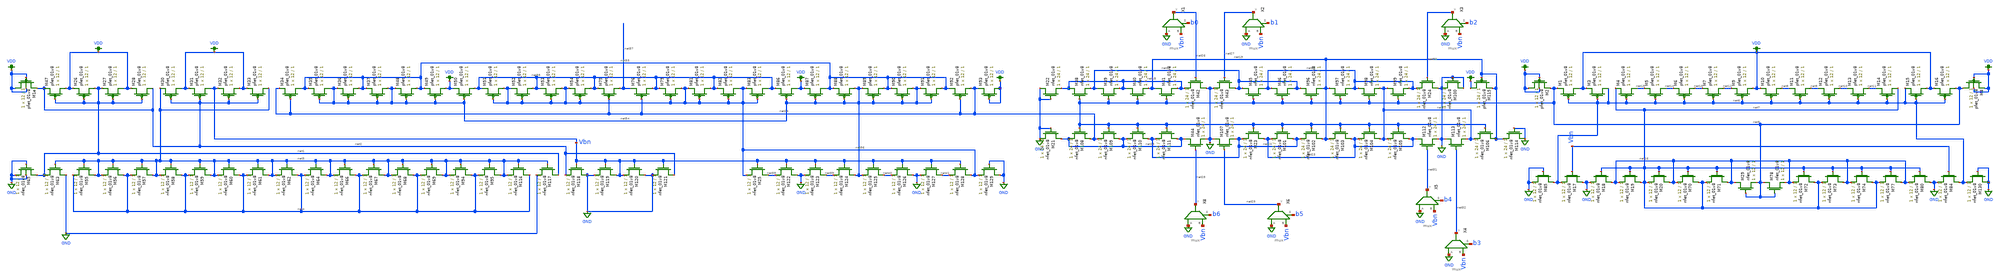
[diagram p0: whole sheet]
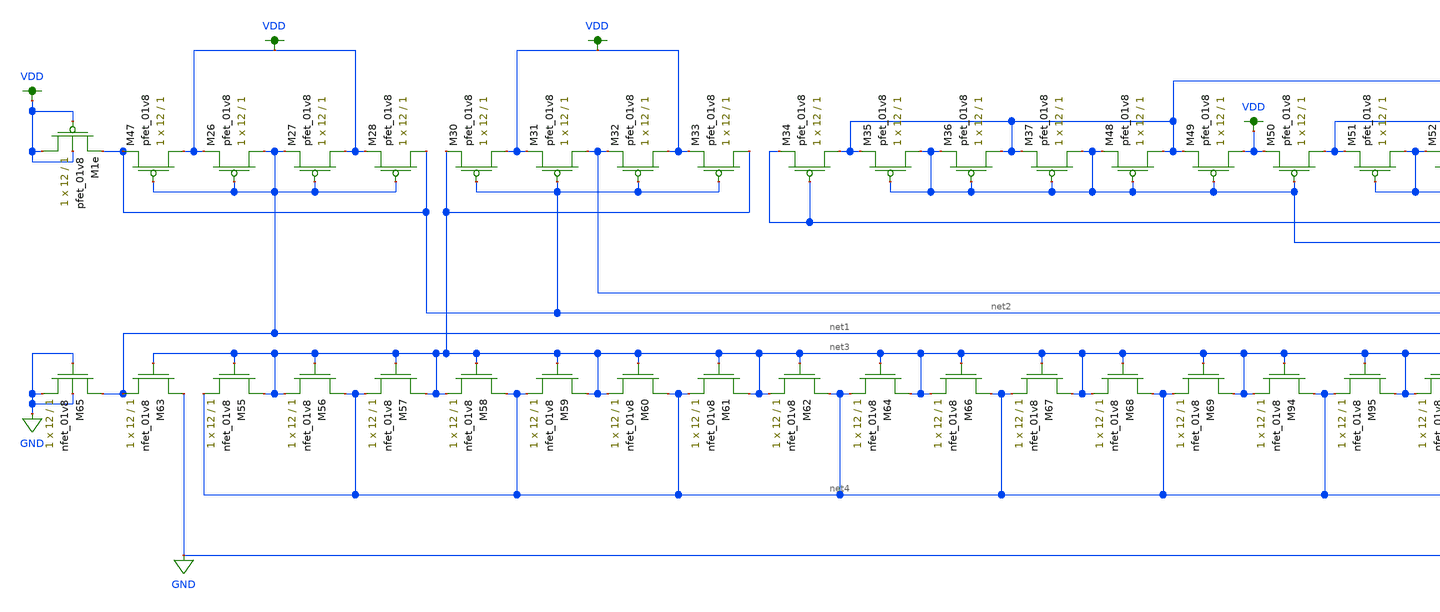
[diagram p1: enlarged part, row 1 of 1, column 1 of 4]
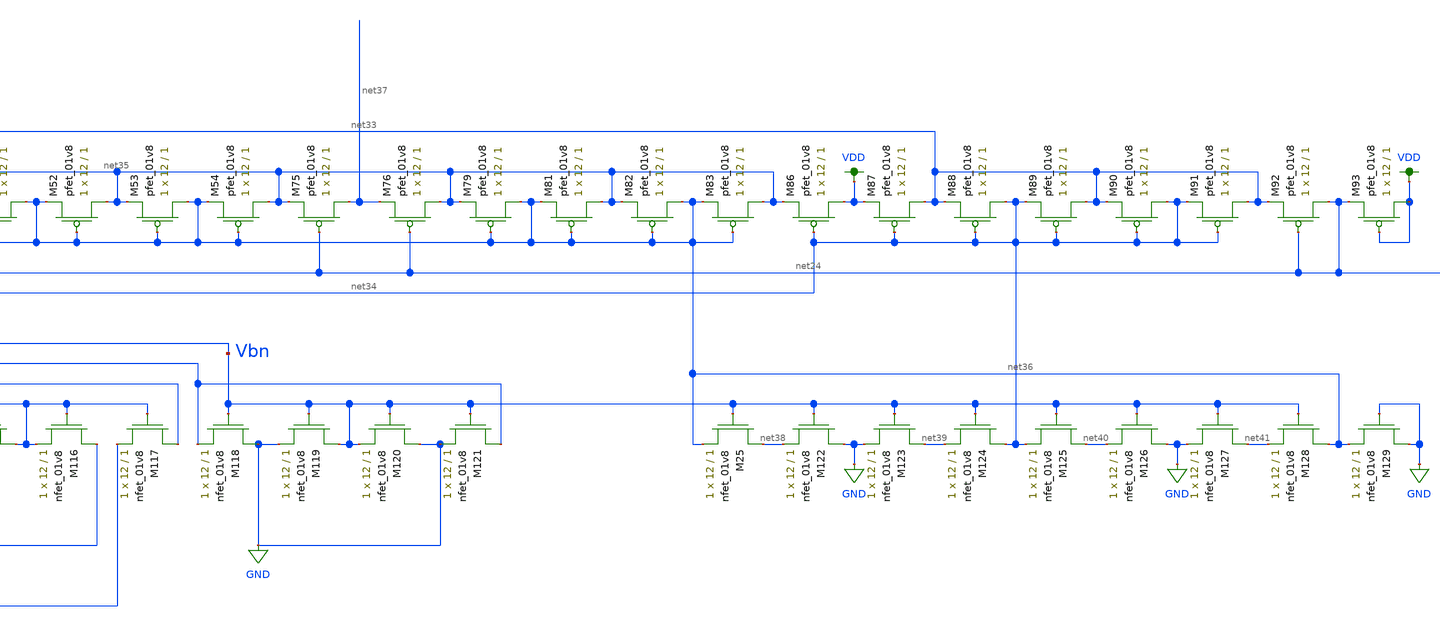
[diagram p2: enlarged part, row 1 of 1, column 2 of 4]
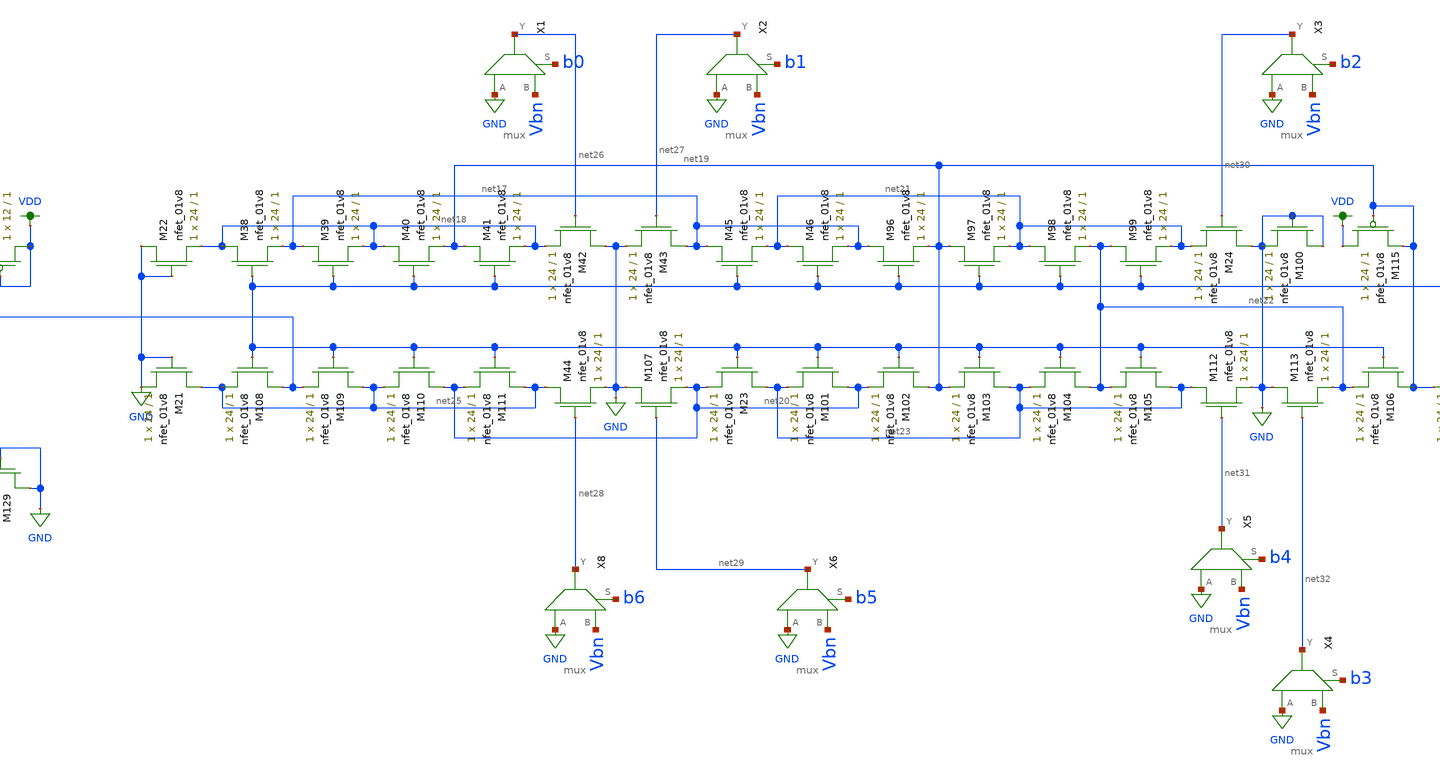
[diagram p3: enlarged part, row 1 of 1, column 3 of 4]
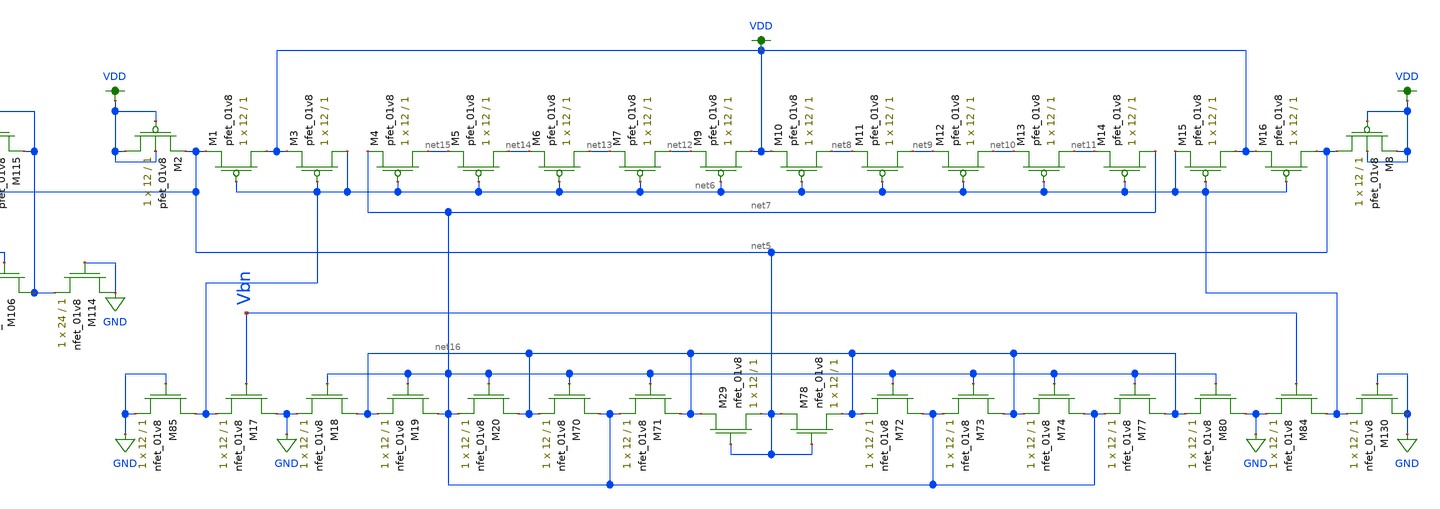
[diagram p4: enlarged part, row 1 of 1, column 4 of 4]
** sch_path: dac/schematics/lds_for_lvs.sch
**.subckt lds_for_lvs
XM47 VDD net1 net2 VDD sky130_fd_pr__pfet_01v8 L=1 W=12 nf=1 ad='int((nf+1)/2) * W/nf * 0.29' as='int((nf+2)/2) * W/nf * 0.29'
+ pd='2*int((nf+1)/2) * (W/nf + 0.29)' ps='2*int((nf+2)/2) * (W/nf + 0.29)' nrd='0.29 / W' nrs='0.29 / W'
+ sa=0 sb=0 sd=0 mult=1 m=1
XM63 GND net3 net1 GND sky130_fd_pr__nfet_01v8 L=1 W=12 nf=1 ad='int((nf+1)/2) * W/nf * 0.29' as='int((nf+2)/2) * W/nf * 0.29'
+ pd='2*int((nf+1)/2) * (W/nf + 0.29)' ps='2*int((nf+2)/2) * (W/nf + 0.29)' nrd='0.29 / W' nrs='0.29 / W'
+ sa=0 sb=0 sd=0 mult=1 m=1
XM1e VDD VDD net2 VDD sky130_fd_pr__pfet_01v8 L=1 W=12 nf=1 ad='int((nf+1)/2) * W/nf * 0.29' as='int((nf+2)/2) * W/nf * 0.29'
+ pd='2*int((nf+1)/2) * (W/nf + 0.29)' ps='2*int((nf+2)/2) * (W/nf + 0.29)' nrd='0.29 / W' nrs='0.29 / W'
+ sa=0 sb=0 sd=0 mult=1 m=1
XM65 net1 GND GND GND sky130_fd_pr__nfet_01v8 L=1 W=12 nf=1 ad='int((nf+1)/2) * W/nf * 0.29' as='int((nf+2)/2) * W/nf * 0.29'
+ pd='2*int((nf+1)/2) * (W/nf + 0.29)' ps='2*int((nf+2)/2) * (W/nf + 0.29)' nrd='0.29 / W' nrs='0.29 / W'
+ sa=0 sb=0 sd=0 mult=1 m=1
XM1 VDD net6 net5 VDD sky130_fd_pr__pfet_01v8 L=1 W=12 nf=1 ad='int((nf+1)/2) * W/nf * 0.29' as='int((nf+2)/2) * W/nf * 0.29'
+ pd='2*int((nf+1)/2) * (W/nf + 0.29)' ps='2*int((nf+2)/2) * (W/nf + 0.29)' nrd='0.29 / W' nrs='0.29 / W'
+ sa=0 sb=0 sd=0 mult=1 m=1
XM2 VDD VDD net5 VDD sky130_fd_pr__pfet_01v8 L=1 W=12 nf=1 ad='int((nf+1)/2) * W/nf * 0.29' as='int((nf+2)/2) * W/nf * 0.29'
+ pd='2*int((nf+1)/2) * (W/nf + 0.29)' ps='2*int((nf+2)/2) * (W/nf + 0.29)' nrd='0.29 / W' nrs='0.29 / W'
+ sa=0 sb=0 sd=0 mult=1 m=1
XM85 net6 GND GND GND sky130_fd_pr__nfet_01v8 L=1 W=12 nf=1 ad='int((nf+1)/2) * W/nf * 0.29' as='int((nf+2)/2) * W/nf * 0.29'
+ pd='2*int((nf+1)/2) * (W/nf + 0.29)' ps='2*int((nf+2)/2) * (W/nf + 0.29)' nrd='0.29 / W' nrs='0.29 / W'
+ sa=0 sb=0 sd=0 mult=1 m=1
X1 GND Vbn net26 b0 mux
X2 GND Vbn net27 b1 mux
X3 GND Vbn net30 b2 mux
X4 GND Vbn net32 b3 mux
X5 GND Vbn net31 b4 mux
X6 GND Vbn net29 b5 mux
X8 GND Vbn net28 b6 mux
XM115 VDD net19 net19 VDD sky130_fd_pr__pfet_01v8 L=1 W=24 nf=1 ad='int((nf+1)/2) * W/nf * 0.29' as='int((nf+2)/2) * W/nf * 0.29'
+ pd='2*int((nf+1)/2) * (W/nf + 0.29)' ps='2*int((nf+2)/2) * (W/nf + 0.29)' nrd='0.29 / W' nrs='0.29 / W'
+ sa=0 sb=0 sd=0 mult=1 m=1
XM22 GND GND net18 GND sky130_fd_pr__nfet_01v8 L=1 W=24 nf=1 ad='int((nf+1)/2) * W/nf * 0.29' as='int((nf+2)/2) * W/nf * 0.29'
+ pd='2*int((nf+1)/2) * (W/nf + 0.29)' ps='2*int((nf+2)/2) * (W/nf + 0.29)' nrd='0.29 / W' nrs='0.29 / W'
+ sa=0 sb=0 sd=0 mult=1 m=1
XM26 net1 net1 VDD VDD sky130_fd_pr__pfet_01v8 L=1 W=12 nf=1 ad='int((nf+1)/2) * W/nf * 0.29' as='int((nf+2)/2) * W/nf * 0.29'
+ pd='2*int((nf+1)/2) * (W/nf + 0.29)' ps='2*int((nf+2)/2) * (W/nf + 0.29)' nrd='0.29 / W' nrs='0.29 / W'
+ sa=0 sb=0 sd=0 mult=1 m=1
XM27 VDD net1 net1 VDD sky130_fd_pr__pfet_01v8 L=1 W=12 nf=1 ad='int((nf+1)/2) * W/nf * 0.29' as='int((nf+2)/2) * W/nf * 0.29'
+ pd='2*int((nf+1)/2) * (W/nf + 0.29)' ps='2*int((nf+2)/2) * (W/nf + 0.29)' nrd='0.29 / W' nrs='0.29 / W'
+ sa=0 sb=0 sd=0 mult=1 m=1
XM28 net2 net1 VDD VDD sky130_fd_pr__pfet_01v8 L=1 W=12 nf=1 ad='int((nf+1)/2) * W/nf * 0.29' as='int((nf+2)/2) * W/nf * 0.29'
+ pd='2*int((nf+1)/2) * (W/nf + 0.29)' ps='2*int((nf+2)/2) * (W/nf + 0.29)' nrd='0.29 / W' nrs='0.29 / W'
+ sa=0 sb=0 sd=0 mult=1 m=1
XM30 VDD net2 net3 VDD sky130_fd_pr__pfet_01v8 L=1 W=12 nf=1 ad='int((nf+1)/2) * W/nf * 0.29' as='int((nf+2)/2) * W/nf * 0.29'
+ pd='2*int((nf+1)/2) * (W/nf + 0.29)' ps='2*int((nf+2)/2) * (W/nf + 0.29)' nrd='0.29 / W' nrs='0.29 / W'
+ sa=0 sb=0 sd=0 mult=1 m=1
XM31 Vbn net2 VDD VDD sky130_fd_pr__pfet_01v8 L=1 W=12 nf=1 ad='int((nf+1)/2) * W/nf * 0.29' as='int((nf+2)/2) * W/nf * 0.29'
+ pd='2*int((nf+1)/2) * (W/nf + 0.29)' ps='2*int((nf+2)/2) * (W/nf + 0.29)' nrd='0.29 / W' nrs='0.29 / W'
+ sa=0 sb=0 sd=0 mult=1 m=1
XM32 VDD net2 Vbn VDD sky130_fd_pr__pfet_01v8 L=1 W=12 nf=1 ad='int((nf+1)/2) * W/nf * 0.29' as='int((nf+2)/2) * W/nf * 0.29'
+ pd='2*int((nf+1)/2) * (W/nf + 0.29)' ps='2*int((nf+2)/2) * (W/nf + 0.29)' nrd='0.29 / W' nrs='0.29 / W'
+ sa=0 sb=0 sd=0 mult=1 m=1
XM33 net3 net2 VDD VDD sky130_fd_pr__pfet_01v8 L=1 W=12 nf=1 ad='int((nf+1)/2) * W/nf * 0.29' as='int((nf+2)/2) * W/nf * 0.29'
+ pd='2*int((nf+1)/2) * (W/nf + 0.29)' ps='2*int((nf+2)/2) * (W/nf + 0.29)' nrd='0.29 / W' nrs='0.29 / W'
+ sa=0 sb=0 sd=0 mult=1 m=1
XM34 net33 net24 net24 VDD sky130_fd_pr__pfet_01v8 L=1 W=12 nf=1 ad='int((nf+1)/2) * W/nf * 0.29' as='int((nf+2)/2) * W/nf * 0.29'
+ pd='2*int((nf+1)/2) * (W/nf + 0.29)' ps='2*int((nf+2)/2) * (W/nf + 0.29)' nrd='0.29 / W' nrs='0.29 / W'
+ sa=0 sb=0 sd=0 mult=1 m=1
XM35 net34 net34 net33 VDD sky130_fd_pr__pfet_01v8 L=1 W=12 nf=1 ad='int((nf+1)/2) * W/nf * 0.29' as='int((nf+2)/2) * W/nf * 0.29'
+ pd='2*int((nf+1)/2) * (W/nf + 0.29)' ps='2*int((nf+2)/2) * (W/nf + 0.29)' nrd='0.29 / W' nrs='0.29 / W'
+ sa=0 sb=0 sd=0 mult=1 m=1
XM36 net33 net34 net34 VDD sky130_fd_pr__pfet_01v8 L=1 W=12 nf=1 ad='int((nf+1)/2) * W/nf * 0.29' as='int((nf+2)/2) * W/nf * 0.29'
+ pd='2*int((nf+1)/2) * (W/nf + 0.29)' ps='2*int((nf+2)/2) * (W/nf + 0.29)' nrd='0.29 / W' nrs='0.29 / W'
+ sa=0 sb=0 sd=0 mult=1 m=1
XM37 net34 net34 net33 VDD sky130_fd_pr__pfet_01v8 L=1 W=12 nf=1 ad='int((nf+1)/2) * W/nf * 0.29' as='int((nf+2)/2) * W/nf * 0.29'
+ pd='2*int((nf+1)/2) * (W/nf + 0.29)' ps='2*int((nf+2)/2) * (W/nf + 0.29)' nrd='0.29 / W' nrs='0.29 / W'
+ sa=0 sb=0 sd=0 mult=1 m=1
XM48 net33 net34 net34 VDD sky130_fd_pr__pfet_01v8 L=1 W=12 nf=1 ad='int((nf+1)/2) * W/nf * 0.29' as='int((nf+2)/2) * W/nf * 0.29'
+ pd='2*int((nf+1)/2) * (W/nf + 0.29)' ps='2*int((nf+2)/2) * (W/nf + 0.29)' nrd='0.29 / W' nrs='0.29 / W'
+ sa=0 sb=0 sd=0 mult=1 m=1
XM49 VDD net34 net33 VDD sky130_fd_pr__pfet_01v8 L=1 W=12 nf=1 ad='int((nf+1)/2) * W/nf * 0.29' as='int((nf+2)/2) * W/nf * 0.29'
+ pd='2*int((nf+1)/2) * (W/nf + 0.29)' ps='2*int((nf+2)/2) * (W/nf + 0.29)' nrd='0.29 / W' nrs='0.29 / W'
+ sa=0 sb=0 sd=0 mult=1 m=1
XM50 net35 net34 VDD VDD sky130_fd_pr__pfet_01v8 L=1 W=12 nf=1 ad='int((nf+1)/2) * W/nf * 0.29' as='int((nf+2)/2) * W/nf * 0.29'
+ pd='2*int((nf+1)/2) * (W/nf + 0.29)' ps='2*int((nf+2)/2) * (W/nf + 0.29)' nrd='0.29 / W' nrs='0.29 / W'
+ sa=0 sb=0 sd=0 mult=1 m=1
XM51 net36 net36 net35 VDD sky130_fd_pr__pfet_01v8 L=1 W=12 nf=1 ad='int((nf+1)/2) * W/nf * 0.29' as='int((nf+2)/2) * W/nf * 0.29'
+ pd='2*int((nf+1)/2) * (W/nf + 0.29)' ps='2*int((nf+2)/2) * (W/nf + 0.29)' nrd='0.29 / W' nrs='0.29 / W'
+ sa=0 sb=0 sd=0 mult=1 m=1
XM52 net35 net36 net36 VDD sky130_fd_pr__pfet_01v8 L=1 W=12 nf=1 ad='int((nf+1)/2) * W/nf * 0.29' as='int((nf+2)/2) * W/nf * 0.29'
+ pd='2*int((nf+1)/2) * (W/nf + 0.29)' ps='2*int((nf+2)/2) * (W/nf + 0.29)' nrd='0.29 / W' nrs='0.29 / W'
+ sa=0 sb=0 sd=0 mult=1 m=1
XM53 net36 net36 net35 VDD sky130_fd_pr__pfet_01v8 L=1 W=12 nf=1 ad='int((nf+1)/2) * W/nf * 0.29' as='int((nf+2)/2) * W/nf * 0.29'
+ pd='2*int((nf+1)/2) * (W/nf + 0.29)' ps='2*int((nf+2)/2) * (W/nf + 0.29)' nrd='0.29 / W' nrs='0.29 / W'
+ sa=0 sb=0 sd=0 mult=1 m=1
XM54 net35 net36 net36 VDD sky130_fd_pr__pfet_01v8 L=1 W=12 nf=1 ad='int((nf+1)/2) * W/nf * 0.29' as='int((nf+2)/2) * W/nf * 0.29'
+ pd='2*int((nf+1)/2) * (W/nf + 0.29)' ps='2*int((nf+2)/2) * (W/nf + 0.29)' nrd='0.29 / W' nrs='0.29 / W'
+ sa=0 sb=0 sd=0 mult=1 m=1
XM75 net37 net24 net35 VDD sky130_fd_pr__pfet_01v8 L=1 W=12 nf=1 ad='int((nf+1)/2) * W/nf * 0.29' as='int((nf+2)/2) * W/nf * 0.29'
+ pd='2*int((nf+1)/2) * (W/nf + 0.29)' ps='2*int((nf+2)/2) * (W/nf + 0.29)' nrd='0.29 / W' nrs='0.29 / W'
+ sa=0 sb=0 sd=0 mult=1 m=1
XM76 net35 net24 net37 VDD sky130_fd_pr__pfet_01v8 L=1 W=12 nf=1 ad='int((nf+1)/2) * W/nf * 0.29' as='int((nf+2)/2) * W/nf * 0.29'
+ pd='2*int((nf+1)/2) * (W/nf + 0.29)' ps='2*int((nf+2)/2) * (W/nf + 0.29)' nrd='0.29 / W' nrs='0.29 / W'
+ sa=0 sb=0 sd=0 mult=1 m=1
XM79 net36 net36 net35 VDD sky130_fd_pr__pfet_01v8 L=1 W=12 nf=1 ad='int((nf+1)/2) * W/nf * 0.29' as='int((nf+2)/2) * W/nf * 0.29'
+ pd='2*int((nf+1)/2) * (W/nf + 0.29)' ps='2*int((nf+2)/2) * (W/nf + 0.29)' nrd='0.29 / W' nrs='0.29 / W'
+ sa=0 sb=0 sd=0 mult=1 m=1
XM81 net35 net36 net36 VDD sky130_fd_pr__pfet_01v8 L=1 W=12 nf=1 ad='int((nf+1)/2) * W/nf * 0.29' as='int((nf+2)/2) * W/nf * 0.29'
+ pd='2*int((nf+1)/2) * (W/nf + 0.29)' ps='2*int((nf+2)/2) * (W/nf + 0.29)' nrd='0.29 / W' nrs='0.29 / W'
+ sa=0 sb=0 sd=0 mult=1 m=1
XM82 net36 net36 net35 VDD sky130_fd_pr__pfet_01v8 L=1 W=12 nf=1 ad='int((nf+1)/2) * W/nf * 0.29' as='int((nf+2)/2) * W/nf * 0.29'
+ pd='2*int((nf+1)/2) * (W/nf + 0.29)' ps='2*int((nf+2)/2) * (W/nf + 0.29)' nrd='0.29 / W' nrs='0.29 / W'
+ sa=0 sb=0 sd=0 mult=1 m=1
XM83 net35 net36 net36 VDD sky130_fd_pr__pfet_01v8 L=1 W=12 nf=1 ad='int((nf+1)/2) * W/nf * 0.29' as='int((nf+2)/2) * W/nf * 0.29'
+ pd='2*int((nf+1)/2) * (W/nf + 0.29)' ps='2*int((nf+2)/2) * (W/nf + 0.29)' nrd='0.29 / W' nrs='0.29 / W'
+ sa=0 sb=0 sd=0 mult=1 m=1
XM86 VDD net34 net35 VDD sky130_fd_pr__pfet_01v8 L=1 W=12 nf=1 ad='int((nf+1)/2) * W/nf * 0.29' as='int((nf+2)/2) * W/nf * 0.29'
+ pd='2*int((nf+1)/2) * (W/nf + 0.29)' ps='2*int((nf+2)/2) * (W/nf + 0.29)' nrd='0.29 / W' nrs='0.29 / W'
+ sa=0 sb=0 sd=0 mult=1 m=1
XM87 net33 net34 VDD VDD sky130_fd_pr__pfet_01v8 L=1 W=12 nf=1 ad='int((nf+1)/2) * W/nf * 0.29' as='int((nf+2)/2) * W/nf * 0.29'
+ pd='2*int((nf+1)/2) * (W/nf + 0.29)' ps='2*int((nf+2)/2) * (W/nf + 0.29)' nrd='0.29 / W' nrs='0.29 / W'
+ sa=0 sb=0 sd=0 mult=1 m=1
XM88 net34 net34 net33 VDD sky130_fd_pr__pfet_01v8 L=1 W=12 nf=1 ad='int((nf+1)/2) * W/nf * 0.29' as='int((nf+2)/2) * W/nf * 0.29'
+ pd='2*int((nf+1)/2) * (W/nf + 0.29)' ps='2*int((nf+2)/2) * (W/nf + 0.29)' nrd='0.29 / W' nrs='0.29 / W'
+ sa=0 sb=0 sd=0 mult=1 m=1
XM89 net33 net34 net34 VDD sky130_fd_pr__pfet_01v8 L=1 W=12 nf=1 ad='int((nf+1)/2) * W/nf * 0.29' as='int((nf+2)/2) * W/nf * 0.29'
+ pd='2*int((nf+1)/2) * (W/nf + 0.29)' ps='2*int((nf+2)/2) * (W/nf + 0.29)' nrd='0.29 / W' nrs='0.29 / W'
+ sa=0 sb=0 sd=0 mult=1 m=1
XM90 net34 net34 net33 VDD sky130_fd_pr__pfet_01v8 L=1 W=12 nf=1 ad='int((nf+1)/2) * W/nf * 0.29' as='int((nf+2)/2) * W/nf * 0.29'
+ pd='2*int((nf+1)/2) * (W/nf + 0.29)' ps='2*int((nf+2)/2) * (W/nf + 0.29)' nrd='0.29 / W' nrs='0.29 / W'
+ sa=0 sb=0 sd=0 mult=1 m=1
XM91 net33 net34 net34 VDD sky130_fd_pr__pfet_01v8 L=1 W=12 nf=1 ad='int((nf+1)/2) * W/nf * 0.29' as='int((nf+2)/2) * W/nf * 0.29'
+ pd='2*int((nf+1)/2) * (W/nf + 0.29)' ps='2*int((nf+2)/2) * (W/nf + 0.29)' nrd='0.29 / W' nrs='0.29 / W'
+ sa=0 sb=0 sd=0 mult=1 m=1
XM92 net24 net24 net33 VDD sky130_fd_pr__pfet_01v8 L=1 W=12 nf=1 ad='int((nf+1)/2) * W/nf * 0.29' as='int((nf+2)/2) * W/nf * 0.29'
+ pd='2*int((nf+1)/2) * (W/nf + 0.29)' ps='2*int((nf+2)/2) * (W/nf + 0.29)' nrd='0.29 / W' nrs='0.29 / W'
+ sa=0 sb=0 sd=0 mult=1 m=1
XM93 VDD VDD net24 VDD sky130_fd_pr__pfet_01v8 L=1 W=12 nf=1 ad='int((nf+1)/2) * W/nf * 0.29' as='int((nf+2)/2) * W/nf * 0.29'
+ pd='2*int((nf+1)/2) * (W/nf + 0.29)' ps='2*int((nf+2)/2) * (W/nf + 0.29)' nrd='0.29 / W' nrs='0.29 / W'
+ sa=0 sb=0 sd=0 mult=1 m=1
XM8 net5 VDD VDD VDD sky130_fd_pr__pfet_01v8 L=1 W=12 nf=1 ad='int((nf+1)/2) * W/nf * 0.29' as='int((nf+2)/2) * W/nf * 0.29'
+ pd='2*int((nf+1)/2) * (W/nf + 0.29)' ps='2*int((nf+2)/2) * (W/nf + 0.29)' nrd='0.29 / W' nrs='0.29 / W'
+ sa=0 sb=0 sd=0 mult=1 m=1
XM3 net6 net6 VDD VDD sky130_fd_pr__pfet_01v8 L=1 W=12 nf=1 ad='int((nf+1)/2) * W/nf * 0.29' as='int((nf+2)/2) * W/nf * 0.29'
+ pd='2*int((nf+1)/2) * (W/nf + 0.29)' ps='2*int((nf+2)/2) * (W/nf + 0.29)' nrd='0.29 / W' nrs='0.29 / W'
+ sa=0 sb=0 sd=0 mult=1 m=1
XM4 net15 net6 net7 VDD sky130_fd_pr__pfet_01v8 L=1 W=12 nf=1 ad='int((nf+1)/2) * W/nf * 0.29' as='int((nf+2)/2) * W/nf * 0.29'
+ pd='2*int((nf+1)/2) * (W/nf + 0.29)' ps='2*int((nf+2)/2) * (W/nf + 0.29)' nrd='0.29 / W' nrs='0.29 / W'
+ sa=0 sb=0 sd=0 mult=1 m=1
XM5 net14 net6 net15 VDD sky130_fd_pr__pfet_01v8 L=1 W=12 nf=1 ad='int((nf+1)/2) * W/nf * 0.29' as='int((nf+2)/2) * W/nf * 0.29'
+ pd='2*int((nf+1)/2) * (W/nf + 0.29)' ps='2*int((nf+2)/2) * (W/nf + 0.29)' nrd='0.29 / W' nrs='0.29 / W'
+ sa=0 sb=0 sd=0 mult=1 m=1
XM6 net13 net6 net14 VDD sky130_fd_pr__pfet_01v8 L=1 W=12 nf=1 ad='int((nf+1)/2) * W/nf * 0.29' as='int((nf+2)/2) * W/nf * 0.29'
+ pd='2*int((nf+1)/2) * (W/nf + 0.29)' ps='2*int((nf+2)/2) * (W/nf + 0.29)' nrd='0.29 / W' nrs='0.29 / W'
+ sa=0 sb=0 sd=0 mult=1 m=1
XM7 net12 net6 net13 VDD sky130_fd_pr__pfet_01v8 L=1 W=12 nf=1 ad='int((nf+1)/2) * W/nf * 0.29' as='int((nf+2)/2) * W/nf * 0.29'
+ pd='2*int((nf+1)/2) * (W/nf + 0.29)' ps='2*int((nf+2)/2) * (W/nf + 0.29)' nrd='0.29 / W' nrs='0.29 / W'
+ sa=0 sb=0 sd=0 mult=1 m=1
XM9 VDD net6 net12 VDD sky130_fd_pr__pfet_01v8 L=1 W=12 nf=1 ad='int((nf+1)/2) * W/nf * 0.29' as='int((nf+2)/2) * W/nf * 0.29'
+ pd='2*int((nf+1)/2) * (W/nf + 0.29)' ps='2*int((nf+2)/2) * (W/nf + 0.29)' nrd='0.29 / W' nrs='0.29 / W'
+ sa=0 sb=0 sd=0 mult=1 m=1
XM10 net8 net6 VDD VDD sky130_fd_pr__pfet_01v8 L=1 W=12 nf=1 ad='int((nf+1)/2) * W/nf * 0.29' as='int((nf+2)/2) * W/nf * 0.29'
+ pd='2*int((nf+1)/2) * (W/nf + 0.29)' ps='2*int((nf+2)/2) * (W/nf + 0.29)' nrd='0.29 / W' nrs='0.29 / W'
+ sa=0 sb=0 sd=0 mult=1 m=1
XM11 net9 net6 net8 VDD sky130_fd_pr__pfet_01v8 L=1 W=12 nf=1 ad='int((nf+1)/2) * W/nf * 0.29' as='int((nf+2)/2) * W/nf * 0.29'
+ pd='2*int((nf+1)/2) * (W/nf + 0.29)' ps='2*int((nf+2)/2) * (W/nf + 0.29)' nrd='0.29 / W' nrs='0.29 / W'
+ sa=0 sb=0 sd=0 mult=1 m=1
XM12 net10 net6 net9 VDD sky130_fd_pr__pfet_01v8 L=1 W=12 nf=1 ad='int((nf+1)/2) * W/nf * 0.29' as='int((nf+2)/2) * W/nf * 0.29'
+ pd='2*int((nf+1)/2) * (W/nf + 0.29)' ps='2*int((nf+2)/2) * (W/nf + 0.29)' nrd='0.29 / W' nrs='0.29 / W'
+ sa=0 sb=0 sd=0 mult=1 m=1
XM13 net11 net6 net10 VDD sky130_fd_pr__pfet_01v8 L=1 W=12 nf=1 ad='int((nf+1)/2) * W/nf * 0.29' as='int((nf+2)/2) * W/nf * 0.29'
+ pd='2*int((nf+1)/2) * (W/nf + 0.29)' ps='2*int((nf+2)/2) * (W/nf + 0.29)' nrd='0.29 / W' nrs='0.29 / W'
+ sa=0 sb=0 sd=0 mult=1 m=1
XM14 net7 net6 net11 VDD sky130_fd_pr__pfet_01v8 L=1 W=12 nf=1 ad='int((nf+1)/2) * W/nf * 0.29' as='int((nf+2)/2) * W/nf * 0.29'
+ pd='2*int((nf+1)/2) * (W/nf + 0.29)' ps='2*int((nf+2)/2) * (W/nf + 0.29)' nrd='0.29 / W' nrs='0.29 / W'
+ sa=0 sb=0 sd=0 mult=1 m=1
XM15 VDD net6 net6 VDD sky130_fd_pr__pfet_01v8 L=1 W=12 nf=1 ad='int((nf+1)/2) * W/nf * 0.29' as='int((nf+2)/2) * W/nf * 0.29'
+ pd='2*int((nf+1)/2) * (W/nf + 0.29)' ps='2*int((nf+2)/2) * (W/nf + 0.29)' nrd='0.29 / W' nrs='0.29 / W'
+ sa=0 sb=0 sd=0 mult=1 m=1
XM16 net5 net6 VDD VDD sky130_fd_pr__pfet_01v8 L=1 W=12 nf=1 ad='int((nf+1)/2) * W/nf * 0.29' as='int((nf+2)/2) * W/nf * 0.29'
+ pd='2*int((nf+1)/2) * (W/nf + 0.29)' ps='2*int((nf+2)/2) * (W/nf + 0.29)' nrd='0.29 / W' nrs='0.29 / W'
+ sa=0 sb=0 sd=0 mult=1 m=1
XM55 net3 net3 net4 GND sky130_fd_pr__nfet_01v8 L=1 W=12 nf=1 ad='int((nf+1)/2) * W/nf * 0.29' as='int((nf+2)/2) * W/nf * 0.29'
+ pd='2*int((nf+1)/2) * (W/nf + 0.29)' ps='2*int((nf+2)/2) * (W/nf + 0.29)' nrd='0.29 / W' nrs='0.29 / W'
+ sa=0 sb=0 sd=0 mult=1 m=1
XM56 net4 net3 net3 GND sky130_fd_pr__nfet_01v8 L=1 W=12 nf=1 ad='int((nf+1)/2) * W/nf * 0.29' as='int((nf+2)/2) * W/nf * 0.29'
+ pd='2*int((nf+1)/2) * (W/nf + 0.29)' ps='2*int((nf+2)/2) * (W/nf + 0.29)' nrd='0.29 / W' nrs='0.29 / W'
+ sa=0 sb=0 sd=0 mult=1 m=1
XM57 net3 net3 net4 GND sky130_fd_pr__nfet_01v8 L=1 W=12 nf=1 ad='int((nf+1)/2) * W/nf * 0.29' as='int((nf+2)/2) * W/nf * 0.29'
+ pd='2*int((nf+1)/2) * (W/nf + 0.29)' ps='2*int((nf+2)/2) * (W/nf + 0.29)' nrd='0.29 / W' nrs='0.29 / W'
+ sa=0 sb=0 sd=0 mult=1 m=1
XM58 net4 net3 net3 GND sky130_fd_pr__nfet_01v8 L=1 W=12 nf=1 ad='int((nf+1)/2) * W/nf * 0.29' as='int((nf+2)/2) * W/nf * 0.29'
+ pd='2*int((nf+1)/2) * (W/nf + 0.29)' ps='2*int((nf+2)/2) * (W/nf + 0.29)' nrd='0.29 / W' nrs='0.29 / W'
+ sa=0 sb=0 sd=0 mult=1 m=1
XM59 net3 net3 net4 GND sky130_fd_pr__nfet_01v8 L=1 W=12 nf=1 ad='int((nf+1)/2) * W/nf * 0.29' as='int((nf+2)/2) * W/nf * 0.29'
+ pd='2*int((nf+1)/2) * (W/nf + 0.29)' ps='2*int((nf+2)/2) * (W/nf + 0.29)' nrd='0.29 / W' nrs='0.29 / W'
+ sa=0 sb=0 sd=0 mult=1 m=1
XM60 net4 net3 net3 GND sky130_fd_pr__nfet_01v8 L=1 W=12 nf=1 ad='int((nf+1)/2) * W/nf * 0.29' as='int((nf+2)/2) * W/nf * 0.29'
+ pd='2*int((nf+1)/2) * (W/nf + 0.29)' ps='2*int((nf+2)/2) * (W/nf + 0.29)' nrd='0.29 / W' nrs='0.29 / W'
+ sa=0 sb=0 sd=0 mult=1 m=1
XM61 net3 net3 net4 GND sky130_fd_pr__nfet_01v8 L=1 W=12 nf=1 ad='int((nf+1)/2) * W/nf * 0.29' as='int((nf+2)/2) * W/nf * 0.29'
+ pd='2*int((nf+1)/2) * (W/nf + 0.29)' ps='2*int((nf+2)/2) * (W/nf + 0.29)' nrd='0.29 / W' nrs='0.29 / W'
+ sa=0 sb=0 sd=0 mult=1 m=1
XM62 net4 net3 net3 GND sky130_fd_pr__nfet_01v8 L=1 W=12 nf=1 ad='int((nf+1)/2) * W/nf * 0.29' as='int((nf+2)/2) * W/nf * 0.29'
+ pd='2*int((nf+1)/2) * (W/nf + 0.29)' ps='2*int((nf+2)/2) * (W/nf + 0.29)' nrd='0.29 / W' nrs='0.29 / W'
+ sa=0 sb=0 sd=0 mult=1 m=1
XM64 net3 net3 net4 GND sky130_fd_pr__nfet_01v8 L=1 W=12 nf=1 ad='int((nf+1)/2) * W/nf * 0.29' as='int((nf+2)/2) * W/nf * 0.29'
+ pd='2*int((nf+1)/2) * (W/nf + 0.29)' ps='2*int((nf+2)/2) * (W/nf + 0.29)' nrd='0.29 / W' nrs='0.29 / W'
+ sa=0 sb=0 sd=0 mult=1 m=1
XM66 net4 net3 net3 GND sky130_fd_pr__nfet_01v8 L=1 W=12 nf=1 ad='int((nf+1)/2) * W/nf * 0.29' as='int((nf+2)/2) * W/nf * 0.29'
+ pd='2*int((nf+1)/2) * (W/nf + 0.29)' ps='2*int((nf+2)/2) * (W/nf + 0.29)' nrd='0.29 / W' nrs='0.29 / W'
+ sa=0 sb=0 sd=0 mult=1 m=1
XM67 net3 net3 net4 GND sky130_fd_pr__nfet_01v8 L=1 W=12 nf=1 ad='int((nf+1)/2) * W/nf * 0.29' as='int((nf+2)/2) * W/nf * 0.29'
+ pd='2*int((nf+1)/2) * (W/nf + 0.29)' ps='2*int((nf+2)/2) * (W/nf + 0.29)' nrd='0.29 / W' nrs='0.29 / W'
+ sa=0 sb=0 sd=0 mult=1 m=1
XM68 net4 net3 net3 GND sky130_fd_pr__nfet_01v8 L=1 W=12 nf=1 ad='int((nf+1)/2) * W/nf * 0.29' as='int((nf+2)/2) * W/nf * 0.29'
+ pd='2*int((nf+1)/2) * (W/nf + 0.29)' ps='2*int((nf+2)/2) * (W/nf + 0.29)' nrd='0.29 / W' nrs='0.29 / W'
+ sa=0 sb=0 sd=0 mult=1 m=1
XM69 net3 net3 net4 GND sky130_fd_pr__nfet_01v8 L=1 W=12 nf=1 ad='int((nf+1)/2) * W/nf * 0.29' as='int((nf+2)/2) * W/nf * 0.29'
+ pd='2*int((nf+1)/2) * (W/nf + 0.29)' ps='2*int((nf+2)/2) * (W/nf + 0.29)' nrd='0.29 / W' nrs='0.29 / W'
+ sa=0 sb=0 sd=0 mult=1 m=1
XM94 net4 net3 net3 GND sky130_fd_pr__nfet_01v8 L=1 W=12 nf=1 ad='int((nf+1)/2) * W/nf * 0.29' as='int((nf+2)/2) * W/nf * 0.29'
+ pd='2*int((nf+1)/2) * (W/nf + 0.29)' ps='2*int((nf+2)/2) * (W/nf + 0.29)' nrd='0.29 / W' nrs='0.29 / W'
+ sa=0 sb=0 sd=0 mult=1 m=1
XM95 net3 net3 net4 GND sky130_fd_pr__nfet_01v8 L=1 W=12 nf=1 ad='int((nf+1)/2) * W/nf * 0.29' as='int((nf+2)/2) * W/nf * 0.29'
+ pd='2*int((nf+1)/2) * (W/nf + 0.29)' ps='2*int((nf+2)/2) * (W/nf + 0.29)' nrd='0.29 / W' nrs='0.29 / W'
+ sa=0 sb=0 sd=0 mult=1 m=1
XM116 net4 net3 net3 GND sky130_fd_pr__nfet_01v8 L=1 W=12 nf=1 ad='int((nf+1)/2) * W/nf * 0.29' as='int((nf+2)/2) * W/nf * 0.29'
+ pd='2*int((nf+1)/2) * (W/nf + 0.29)' ps='2*int((nf+2)/2) * (W/nf + 0.29)' nrd='0.29 / W' nrs='0.29 / W'
+ sa=0 sb=0 sd=0 mult=1 m=1
XM117 net1 net3 GND GND sky130_fd_pr__nfet_01v8 L=1 W=12 nf=1 ad='int((nf+1)/2) * W/nf * 0.29' as='int((nf+2)/2) * W/nf * 0.29'
+ pd='2*int((nf+1)/2) * (W/nf + 0.29)' ps='2*int((nf+2)/2) * (W/nf + 0.29)' nrd='0.29 / W' nrs='0.29 / W'
+ sa=0 sb=0 sd=0 mult=1 m=1
XM118 GND Vbn net2 GND sky130_fd_pr__nfet_01v8 L=1 W=12 nf=1 ad='int((nf+1)/2) * W/nf * 0.29' as='int((nf+2)/2) * W/nf * 0.29'
+ pd='2*int((nf+1)/2) * (W/nf + 0.29)' ps='2*int((nf+2)/2) * (W/nf + 0.29)' nrd='0.29 / W' nrs='0.29 / W'
+ sa=0 sb=0 sd=0 mult=1 m=1
XM119 Vbn Vbn GND GND sky130_fd_pr__nfet_01v8 L=1 W=12 nf=1 ad='int((nf+1)/2) * W/nf * 0.29' as='int((nf+2)/2) * W/nf * 0.29'
+ pd='2*int((nf+1)/2) * (W/nf + 0.29)' ps='2*int((nf+2)/2) * (W/nf + 0.29)' nrd='0.29 / W' nrs='0.29 / W'
+ sa=0 sb=0 sd=0 mult=1 m=1
XM120 GND Vbn Vbn GND sky130_fd_pr__nfet_01v8 L=1 W=12 nf=1 ad='int((nf+1)/2) * W/nf * 0.29' as='int((nf+2)/2) * W/nf * 0.29'
+ pd='2*int((nf+1)/2) * (W/nf + 0.29)' ps='2*int((nf+2)/2) * (W/nf + 0.29)' nrd='0.29 / W' nrs='0.29 / W'
+ sa=0 sb=0 sd=0 mult=1 m=1
XM121 net2 Vbn GND GND sky130_fd_pr__nfet_01v8 L=1 W=12 nf=1 ad='int((nf+1)/2) * W/nf * 0.29' as='int((nf+2)/2) * W/nf * 0.29'
+ pd='2*int((nf+1)/2) * (W/nf + 0.29)' ps='2*int((nf+2)/2) * (W/nf + 0.29)' nrd='0.29 / W' nrs='0.29 / W'
+ sa=0 sb=0 sd=0 mult=1 m=1
XM25 net38 Vbn net36 GND sky130_fd_pr__nfet_01v8 L=1 W=12 nf=1 ad='int((nf+1)/2) * W/nf * 0.29' as='int((nf+2)/2) * W/nf * 0.29'
+ pd='2*int((nf+1)/2) * (W/nf + 0.29)' ps='2*int((nf+2)/2) * (W/nf + 0.29)' nrd='0.29 / W' nrs='0.29 / W'
+ sa=0 sb=0 sd=0 mult=1 m=1
XM122 GND Vbn net38 GND sky130_fd_pr__nfet_01v8 L=1 W=12 nf=1 ad='int((nf+1)/2) * W/nf * 0.29' as='int((nf+2)/2) * W/nf * 0.29'
+ pd='2*int((nf+1)/2) * (W/nf + 0.29)' ps='2*int((nf+2)/2) * (W/nf + 0.29)' nrd='0.29 / W' nrs='0.29 / W'
+ sa=0 sb=0 sd=0 mult=1 m=1
XM123 net39 Vbn GND GND sky130_fd_pr__nfet_01v8 L=1 W=12 nf=1 ad='int((nf+1)/2) * W/nf * 0.29' as='int((nf+2)/2) * W/nf * 0.29'
+ pd='2*int((nf+1)/2) * (W/nf + 0.29)' ps='2*int((nf+2)/2) * (W/nf + 0.29)' nrd='0.29 / W' nrs='0.29 / W'
+ sa=0 sb=0 sd=0 mult=1 m=1
XM124 net34 Vbn net39 GND sky130_fd_pr__nfet_01v8 L=1 W=12 nf=1 ad='int((nf+1)/2) * W/nf * 0.29' as='int((nf+2)/2) * W/nf * 0.29'
+ pd='2*int((nf+1)/2) * (W/nf + 0.29)' ps='2*int((nf+2)/2) * (W/nf + 0.29)' nrd='0.29 / W' nrs='0.29 / W'
+ sa=0 sb=0 sd=0 mult=1 m=1
XM125 net40 Vbn net34 GND sky130_fd_pr__nfet_01v8 L=1 W=12 nf=1 ad='int((nf+1)/2) * W/nf * 0.29' as='int((nf+2)/2) * W/nf * 0.29'
+ pd='2*int((nf+1)/2) * (W/nf + 0.29)' ps='2*int((nf+2)/2) * (W/nf + 0.29)' nrd='0.29 / W' nrs='0.29 / W'
+ sa=0 sb=0 sd=0 mult=1 m=1
XM126 GND Vbn net40 GND sky130_fd_pr__nfet_01v8 L=1 W=12 nf=1 ad='int((nf+1)/2) * W/nf * 0.29' as='int((nf+2)/2) * W/nf * 0.29'
+ pd='2*int((nf+1)/2) * (W/nf + 0.29)' ps='2*int((nf+2)/2) * (W/nf + 0.29)' nrd='0.29 / W' nrs='0.29 / W'
+ sa=0 sb=0 sd=0 mult=1 m=1
XM127 net41 Vbn GND GND sky130_fd_pr__nfet_01v8 L=1 W=12 nf=1 ad='int((nf+1)/2) * W/nf * 0.29' as='int((nf+2)/2) * W/nf * 0.29'
+ pd='2*int((nf+1)/2) * (W/nf + 0.29)' ps='2*int((nf+2)/2) * (W/nf + 0.29)' nrd='0.29 / W' nrs='0.29 / W'
+ sa=0 sb=0 sd=0 mult=1 m=1
XM128 net36 Vbn net41 GND sky130_fd_pr__nfet_01v8 L=1 W=12 nf=1 ad='int((nf+1)/2) * W/nf * 0.29' as='int((nf+2)/2) * W/nf * 0.29'
+ pd='2*int((nf+1)/2) * (W/nf + 0.29)' ps='2*int((nf+2)/2) * (W/nf + 0.29)' nrd='0.29 / W' nrs='0.29 / W'
+ sa=0 sb=0 sd=0 mult=1 m=1
XM129 GND GND net36 GND sky130_fd_pr__nfet_01v8 L=1 W=12 nf=1 ad='int((nf+1)/2) * W/nf * 0.29' as='int((nf+2)/2) * W/nf * 0.29'
+ pd='2*int((nf+1)/2) * (W/nf + 0.29)' ps='2*int((nf+2)/2) * (W/nf + 0.29)' nrd='0.29 / W' nrs='0.29 / W'
+ sa=0 sb=0 sd=0 mult=1 m=1
XM38 net18 net5 net17 GND sky130_fd_pr__nfet_01v8 L=1 W=24 nf=1 ad='int((nf+1)/2) * W/nf * 0.29' as='int((nf+2)/2) * W/nf * 0.29'
+ pd='2*int((nf+1)/2) * (W/nf + 0.29)' ps='2*int((nf+2)/2) * (W/nf + 0.29)' nrd='0.29 / W' nrs='0.29 / W'
+ sa=0 sb=0 sd=0 mult=1 m=1
XM39 net17 net5 net18 GND sky130_fd_pr__nfet_01v8 L=1 W=24 nf=1 ad='int((nf+1)/2) * W/nf * 0.29' as='int((nf+2)/2) * W/nf * 0.29'
+ pd='2*int((nf+1)/2) * (W/nf + 0.29)' ps='2*int((nf+2)/2) * (W/nf + 0.29)' nrd='0.29 / W' nrs='0.29 / W'
+ sa=0 sb=0 sd=0 mult=1 m=1
XM40 net18 net5 net19 GND sky130_fd_pr__nfet_01v8 L=1 W=24 nf=1 ad='int((nf+1)/2) * W/nf * 0.29' as='int((nf+2)/2) * W/nf * 0.29'
+ pd='2*int((nf+1)/2) * (W/nf + 0.29)' ps='2*int((nf+2)/2) * (W/nf + 0.29)' nrd='0.29 / W' nrs='0.29 / W'
+ sa=0 sb=0 sd=0 mult=1 m=1
XM41 net19 net5 net18 GND sky130_fd_pr__nfet_01v8 L=1 W=24 nf=1 ad='int((nf+1)/2) * W/nf * 0.29' as='int((nf+2)/2) * W/nf * 0.29'
+ pd='2*int((nf+1)/2) * (W/nf + 0.29)' ps='2*int((nf+2)/2) * (W/nf + 0.29)' nrd='0.29 / W' nrs='0.29 / W'
+ sa=0 sb=0 sd=0 mult=1 m=1
XM42 GND net26 net18 GND sky130_fd_pr__nfet_01v8 L=1 W=24 nf=1 ad='int((nf+1)/2) * W/nf * 0.29' as='int((nf+2)/2) * W/nf * 0.29'
+ pd='2*int((nf+1)/2) * (W/nf + 0.29)' ps='2*int((nf+2)/2) * (W/nf + 0.29)' nrd='0.29 / W' nrs='0.29 / W'
+ sa=0 sb=0 sd=0 mult=1 m=1
XM43 net17 net27 GND GND sky130_fd_pr__nfet_01v8 L=1 W=24 nf=1 ad='int((nf+1)/2) * W/nf * 0.29' as='int((nf+2)/2) * W/nf * 0.29'
+ pd='2*int((nf+1)/2) * (W/nf + 0.29)' ps='2*int((nf+2)/2) * (W/nf + 0.29)' nrd='0.29 / W' nrs='0.29 / W'
+ sa=0 sb=0 sd=0 mult=1 m=1
XM45 net17 net5 net21 GND sky130_fd_pr__nfet_01v8 L=1 W=24 nf=1 ad='int((nf+1)/2) * W/nf * 0.29' as='int((nf+2)/2) * W/nf * 0.29'
+ pd='2*int((nf+1)/2) * (W/nf + 0.29)' ps='2*int((nf+2)/2) * (W/nf + 0.29)' nrd='0.29 / W' nrs='0.29 / W'
+ sa=0 sb=0 sd=0 mult=1 m=1
XM46 net21 net5 net17 GND sky130_fd_pr__nfet_01v8 L=1 W=24 nf=1 ad='int((nf+1)/2) * W/nf * 0.29' as='int((nf+2)/2) * W/nf * 0.29'
+ pd='2*int((nf+1)/2) * (W/nf + 0.29)' ps='2*int((nf+2)/2) * (W/nf + 0.29)' nrd='0.29 / W' nrs='0.29 / W'
+ sa=0 sb=0 sd=0 mult=1 m=1
XM96 net17 net5 net19 GND sky130_fd_pr__nfet_01v8 L=1 W=24 nf=1 ad='int((nf+1)/2) * W/nf * 0.29' as='int((nf+2)/2) * W/nf * 0.29'
+ pd='2*int((nf+1)/2) * (W/nf + 0.29)' ps='2*int((nf+2)/2) * (W/nf + 0.29)' nrd='0.29 / W' nrs='0.29 / W'
+ sa=0 sb=0 sd=0 mult=1 m=1
XM97 net19 net5 net21 GND sky130_fd_pr__nfet_01v8 L=1 W=24 nf=1 ad='int((nf+1)/2) * W/nf * 0.29' as='int((nf+2)/2) * W/nf * 0.29'
+ pd='2*int((nf+1)/2) * (W/nf + 0.29)' ps='2*int((nf+2)/2) * (W/nf + 0.29)' nrd='0.29 / W' nrs='0.29 / W'
+ sa=0 sb=0 sd=0 mult=1 m=1
XM98 net21 net5 net22 GND sky130_fd_pr__nfet_01v8 L=1 W=24 nf=1 ad='int((nf+1)/2) * W/nf * 0.29' as='int((nf+2)/2) * W/nf * 0.29'
+ pd='2*int((nf+1)/2) * (W/nf + 0.29)' ps='2*int((nf+2)/2) * (W/nf + 0.29)' nrd='0.29 / W' nrs='0.29 / W'
+ sa=0 sb=0 sd=0 mult=1 m=1
XM99 net22 net5 net21 GND sky130_fd_pr__nfet_01v8 L=1 W=24 nf=1 ad='int((nf+1)/2) * W/nf * 0.29' as='int((nf+2)/2) * W/nf * 0.29'
+ pd='2*int((nf+1)/2) * (W/nf + 0.29)' ps='2*int((nf+2)/2) * (W/nf + 0.29)' nrd='0.29 / W' nrs='0.29 / W'
+ sa=0 sb=0 sd=0 mult=1 m=1
XM24 GND net30 net21 GND sky130_fd_pr__nfet_01v8 L=1 W=24 nf=1 ad='int((nf+1)/2) * W/nf * 0.29' as='int((nf+2)/2) * W/nf * 0.29'
+ pd='2*int((nf+1)/2) * (W/nf + 0.29)' ps='2*int((nf+2)/2) * (W/nf + 0.29)' nrd='0.29 / W' nrs='0.29 / W'
+ sa=0 sb=0 sd=0 mult=1 m=1
XM100 GND GND GND GND sky130_fd_pr__nfet_01v8 L=1 W=24 nf=1 ad='int((nf+1)/2) * W/nf * 0.29' as='int((nf+2)/2) * W/nf * 0.29'
+ pd='2*int((nf+1)/2) * (W/nf + 0.29)' ps='2*int((nf+2)/2) * (W/nf + 0.29)' nrd='0.29 / W' nrs='0.29 / W'
+ sa=0 sb=0 sd=0 mult=1 m=1
XM21 net25 GND GND GND sky130_fd_pr__nfet_01v8 L=1 W=24 nf=1 ad='int((nf+1)/2) * W/nf * 0.29' as='int((nf+2)/2) * W/nf * 0.29'
+ pd='2*int((nf+1)/2) * (W/nf + 0.29)' ps='2*int((nf+2)/2) * (W/nf + 0.29)' nrd='0.29 / W' nrs='0.29 / W'
+ sa=0 sb=0 sd=0 mult=1 m=1
XM108 net24 net5 net25 GND sky130_fd_pr__nfet_01v8 L=1 W=24 nf=1 ad='int((nf+1)/2) * W/nf * 0.29' as='int((nf+2)/2) * W/nf * 0.29'
+ pd='2*int((nf+1)/2) * (W/nf + 0.29)' ps='2*int((nf+2)/2) * (W/nf + 0.29)' nrd='0.29 / W' nrs='0.29 / W'
+ sa=0 sb=0 sd=0 mult=1 m=1
XM109 net25 net5 net24 GND sky130_fd_pr__nfet_01v8 L=1 W=24 nf=1 ad='int((nf+1)/2) * W/nf * 0.29' as='int((nf+2)/2) * W/nf * 0.29'
+ pd='2*int((nf+1)/2) * (W/nf + 0.29)' ps='2*int((nf+2)/2) * (W/nf + 0.29)' nrd='0.29 / W' nrs='0.29 / W'
+ sa=0 sb=0 sd=0 mult=1 m=1
XM110 net20 net5 net25 GND sky130_fd_pr__nfet_01v8 L=1 W=24 nf=1 ad='int((nf+1)/2) * W/nf * 0.29' as='int((nf+2)/2) * W/nf * 0.29'
+ pd='2*int((nf+1)/2) * (W/nf + 0.29)' ps='2*int((nf+2)/2) * (W/nf + 0.29)' nrd='0.29 / W' nrs='0.29 / W'
+ sa=0 sb=0 sd=0 mult=1 m=1
XM111 net25 net5 net20 GND sky130_fd_pr__nfet_01v8 L=1 W=24 nf=1 ad='int((nf+1)/2) * W/nf * 0.29' as='int((nf+2)/2) * W/nf * 0.29'
+ pd='2*int((nf+1)/2) * (W/nf + 0.29)' ps='2*int((nf+2)/2) * (W/nf + 0.29)' nrd='0.29 / W' nrs='0.29 / W'
+ sa=0 sb=0 sd=0 mult=1 m=1
XM44 net25 net28 GND GND sky130_fd_pr__nfet_01v8 L=1 W=24 nf=1 ad='int((nf+1)/2) * W/nf * 0.29' as='int((nf+2)/2) * W/nf * 0.29'
+ pd='2*int((nf+1)/2) * (W/nf + 0.29)' ps='2*int((nf+2)/2) * (W/nf + 0.29)' nrd='0.29 / W' nrs='0.29 / W'
+ sa=0 sb=0 sd=0 mult=1 m=1
XM107 GND net29 net20 GND sky130_fd_pr__nfet_01v8 L=1 W=24 nf=1 ad='int((nf+1)/2) * W/nf * 0.29' as='int((nf+2)/2) * W/nf * 0.29'
+ pd='2*int((nf+1)/2) * (W/nf + 0.29)' ps='2*int((nf+2)/2) * (W/nf + 0.29)' nrd='0.29 / W' nrs='0.29 / W'
+ sa=0 sb=0 sd=0 mult=1 m=1
XM112 net23 net31 GND GND sky130_fd_pr__nfet_01v8 L=1 W=24 nf=1 ad='int((nf+1)/2) * W/nf * 0.29' as='int((nf+2)/2) * W/nf * 0.29'
+ pd='2*int((nf+1)/2) * (W/nf + 0.29)' ps='2*int((nf+2)/2) * (W/nf + 0.29)' nrd='0.29 / W' nrs='0.29 / W'
+ sa=0 sb=0 sd=0 mult=1 m=1
XM113 GND net32 net22 GND sky130_fd_pr__nfet_01v8 L=1 W=24 nf=1 ad='int((nf+1)/2) * W/nf * 0.29' as='int((nf+2)/2) * W/nf * 0.29'
+ pd='2*int((nf+1)/2) * (W/nf + 0.29)' ps='2*int((nf+2)/2) * (W/nf + 0.29)' nrd='0.29 / W' nrs='0.29 / W'
+ sa=0 sb=0 sd=0 mult=1 m=1
XM23 net23 net5 net20 GND sky130_fd_pr__nfet_01v8 L=1 W=24 nf=1 ad='int((nf+1)/2) * W/nf * 0.29' as='int((nf+2)/2) * W/nf * 0.29'
+ pd='2*int((nf+1)/2) * (W/nf + 0.29)' ps='2*int((nf+2)/2) * (W/nf + 0.29)' nrd='0.29 / W' nrs='0.29 / W'
+ sa=0 sb=0 sd=0 mult=1 m=1
XM101 net20 net5 net23 GND sky130_fd_pr__nfet_01v8 L=1 W=24 nf=1 ad='int((nf+1)/2) * W/nf * 0.29' as='int((nf+2)/2) * W/nf * 0.29'
+ pd='2*int((nf+1)/2) * (W/nf + 0.29)' ps='2*int((nf+2)/2) * (W/nf + 0.29)' nrd='0.29 / W' nrs='0.29 / W'
+ sa=0 sb=0 sd=0 mult=1 m=1
XM102 net19 net5 net20 GND sky130_fd_pr__nfet_01v8 L=1 W=24 nf=1 ad='int((nf+1)/2) * W/nf * 0.29' as='int((nf+2)/2) * W/nf * 0.29'
+ pd='2*int((nf+1)/2) * (W/nf + 0.29)' ps='2*int((nf+2)/2) * (W/nf + 0.29)' nrd='0.29 / W' nrs='0.29 / W'
+ sa=0 sb=0 sd=0 mult=1 m=1
XM103 net23 net5 net19 GND sky130_fd_pr__nfet_01v8 L=1 W=24 nf=1 ad='int((nf+1)/2) * W/nf * 0.29' as='int((nf+2)/2) * W/nf * 0.29'
+ pd='2*int((nf+1)/2) * (W/nf + 0.29)' ps='2*int((nf+2)/2) * (W/nf + 0.29)' nrd='0.29 / W' nrs='0.29 / W'
+ sa=0 sb=0 sd=0 mult=1 m=1
XM104 net22 net5 net23 GND sky130_fd_pr__nfet_01v8 L=1 W=24 nf=1 ad='int((nf+1)/2) * W/nf * 0.29' as='int((nf+2)/2) * W/nf * 0.29'
+ pd='2*int((nf+1)/2) * (W/nf + 0.29)' ps='2*int((nf+2)/2) * (W/nf + 0.29)' nrd='0.29 / W' nrs='0.29 / W'
+ sa=0 sb=0 sd=0 mult=1 m=1
XM105 net23 net5 net22 GND sky130_fd_pr__nfet_01v8 L=1 W=24 nf=1 ad='int((nf+1)/2) * W/nf * 0.29' as='int((nf+2)/2) * W/nf * 0.29'
+ pd='2*int((nf+1)/2) * (W/nf + 0.29)' ps='2*int((nf+2)/2) * (W/nf + 0.29)' nrd='0.29 / W' nrs='0.29 / W'
+ sa=0 sb=0 sd=0 mult=1 m=1
XM106 net19 net5 net22 GND sky130_fd_pr__nfet_01v8 L=1 W=24 nf=1 ad='int((nf+1)/2) * W/nf * 0.29' as='int((nf+2)/2) * W/nf * 0.29'
+ pd='2*int((nf+1)/2) * (W/nf + 0.29)' ps='2*int((nf+2)/2) * (W/nf + 0.29)' nrd='0.29 / W' nrs='0.29 / W'
+ sa=0 sb=0 sd=0 mult=1 m=1
XM114 GND GND net19 GND sky130_fd_pr__nfet_01v8 L=1 W=24 nf=1 ad='int((nf+1)/2) * W/nf * 0.29' as='int((nf+2)/2) * W/nf * 0.29'
+ pd='2*int((nf+1)/2) * (W/nf + 0.29)' ps='2*int((nf+2)/2) * (W/nf + 0.29)' nrd='0.29 / W' nrs='0.29 / W'
+ sa=0 sb=0 sd=0 mult=1 m=1
XM17 GND Vbn net6 GND sky130_fd_pr__nfet_01v8 L=1 W=12 nf=1 ad='int((nf+1)/2) * W/nf * 0.29' as='int((nf+2)/2) * W/nf * 0.29'
+ pd='2*int((nf+1)/2) * (W/nf + 0.29)' ps='2*int((nf+2)/2) * (W/nf + 0.29)' nrd='0.29 / W' nrs='0.29 / W'
+ sa=0 sb=0 sd=0 mult=1 m=1
XM18 net16 net7 GND GND sky130_fd_pr__nfet_01v8 L=1 W=12 nf=1 ad='int((nf+1)/2) * W/nf * 0.29' as='int((nf+2)/2) * W/nf * 0.29'
+ pd='2*int((nf+1)/2) * (W/nf + 0.29)' ps='2*int((nf+2)/2) * (W/nf + 0.29)' nrd='0.29 / W' nrs='0.29 / W'
+ sa=0 sb=0 sd=0 mult=1 m=1
XM19 net7 net7 net16 GND sky130_fd_pr__nfet_01v8 L=1 W=12 nf=1 ad='int((nf+1)/2) * W/nf * 0.29' as='int((nf+2)/2) * W/nf * 0.29'
+ pd='2*int((nf+1)/2) * (W/nf + 0.29)' ps='2*int((nf+2)/2) * (W/nf + 0.29)' nrd='0.29 / W' nrs='0.29 / W'
+ sa=0 sb=0 sd=0 mult=1 m=1
XM20 net16 net7 net7 GND sky130_fd_pr__nfet_01v8 L=1 W=12 nf=1 ad='int((nf+1)/2) * W/nf * 0.29' as='int((nf+2)/2) * W/nf * 0.29'
+ pd='2*int((nf+1)/2) * (W/nf + 0.29)' ps='2*int((nf+2)/2) * (W/nf + 0.29)' nrd='0.29 / W' nrs='0.29 / W'
+ sa=0 sb=0 sd=0 mult=1 m=1
XM70 net7 net7 net16 GND sky130_fd_pr__nfet_01v8 L=1 W=12 nf=1 ad='int((nf+1)/2) * W/nf * 0.29' as='int((nf+2)/2) * W/nf * 0.29'
+ pd='2*int((nf+1)/2) * (W/nf + 0.29)' ps='2*int((nf+2)/2) * (W/nf + 0.29)' nrd='0.29 / W' nrs='0.29 / W'
+ sa=0 sb=0 sd=0 mult=1 m=1
XM71 net16 net7 net7 GND sky130_fd_pr__nfet_01v8 L=1 W=12 nf=1 ad='int((nf+1)/2) * W/nf * 0.29' as='int((nf+2)/2) * W/nf * 0.29'
+ pd='2*int((nf+1)/2) * (W/nf + 0.29)' ps='2*int((nf+2)/2) * (W/nf + 0.29)' nrd='0.29 / W' nrs='0.29 / W'
+ sa=0 sb=0 sd=0 mult=1 m=1
XM29 net16 net5 net5 GND sky130_fd_pr__nfet_01v8 L=1 W=12 nf=1 ad='int((nf+1)/2) * W/nf * 0.29' as='int((nf+2)/2) * W/nf * 0.29'
+ pd='2*int((nf+1)/2) * (W/nf + 0.29)' ps='2*int((nf+2)/2) * (W/nf + 0.29)' nrd='0.29 / W' nrs='0.29 / W'
+ sa=0 sb=0 sd=0 mult=1 m=1
XM78 net5 net5 net16 GND sky130_fd_pr__nfet_01v8 L=1 W=12 nf=1 ad='int((nf+1)/2) * W/nf * 0.29' as='int((nf+2)/2) * W/nf * 0.29'
+ pd='2*int((nf+1)/2) * (W/nf + 0.29)' ps='2*int((nf+2)/2) * (W/nf + 0.29)' nrd='0.29 / W' nrs='0.29 / W'
+ sa=0 sb=0 sd=0 mult=1 m=1
XM72 net7 net7 net16 GND sky130_fd_pr__nfet_01v8 L=1 W=12 nf=1 ad='int((nf+1)/2) * W/nf * 0.29' as='int((nf+2)/2) * W/nf * 0.29'
+ pd='2*int((nf+1)/2) * (W/nf + 0.29)' ps='2*int((nf+2)/2) * (W/nf + 0.29)' nrd='0.29 / W' nrs='0.29 / W'
+ sa=0 sb=0 sd=0 mult=1 m=1
XM73 net16 net7 net7 GND sky130_fd_pr__nfet_01v8 L=1 W=12 nf=1 ad='int((nf+1)/2) * W/nf * 0.29' as='int((nf+2)/2) * W/nf * 0.29'
+ pd='2*int((nf+1)/2) * (W/nf + 0.29)' ps='2*int((nf+2)/2) * (W/nf + 0.29)' nrd='0.29 / W' nrs='0.29 / W'
+ sa=0 sb=0 sd=0 mult=1 m=1
XM74 net7 net7 net16 GND sky130_fd_pr__nfet_01v8 L=1 W=12 nf=1 ad='int((nf+1)/2) * W/nf * 0.29' as='int((nf+2)/2) * W/nf * 0.29'
+ pd='2*int((nf+1)/2) * (W/nf + 0.29)' ps='2*int((nf+2)/2) * (W/nf + 0.29)' nrd='0.29 / W' nrs='0.29 / W'
+ sa=0 sb=0 sd=0 mult=1 m=1
XM77 net16 net7 net7 GND sky130_fd_pr__nfet_01v8 L=1 W=12 nf=1 ad='int((nf+1)/2) * W/nf * 0.29' as='int((nf+2)/2) * W/nf * 0.29'
+ pd='2*int((nf+1)/2) * (W/nf + 0.29)' ps='2*int((nf+2)/2) * (W/nf + 0.29)' nrd='0.29 / W' nrs='0.29 / W'
+ sa=0 sb=0 sd=0 mult=1 m=1
XM80 GND net7 net16 GND sky130_fd_pr__nfet_01v8 L=1 W=12 nf=1 ad='int((nf+1)/2) * W/nf * 0.29' as='int((nf+2)/2) * W/nf * 0.29'
+ pd='2*int((nf+1)/2) * (W/nf + 0.29)' ps='2*int((nf+2)/2) * (W/nf + 0.29)' nrd='0.29 / W' nrs='0.29 / W'
+ sa=0 sb=0 sd=0 mult=1 m=1
XM84 net6 Vbn GND GND sky130_fd_pr__nfet_01v8 L=1 W=12 nf=1 ad='int((nf+1)/2) * W/nf * 0.29' as='int((nf+2)/2) * W/nf * 0.29'
+ pd='2*int((nf+1)/2) * (W/nf + 0.29)' ps='2*int((nf+2)/2) * (W/nf + 0.29)' nrd='0.29 / W' nrs='0.29 / W'
+ sa=0 sb=0 sd=0 mult=1 m=1
XM130 GND GND net6 GND sky130_fd_pr__nfet_01v8 L=1 W=12 nf=1 ad='int((nf+1)/2) * W/nf * 0.29' as='int((nf+2)/2) * W/nf * 0.29'
+ pd='2*int((nf+1)/2) * (W/nf + 0.29)' ps='2*int((nf+2)/2) * (W/nf + 0.29)' nrd='0.29 / W' nrs='0.29 / W'
+ sa=0 sb=0 sd=0 mult=1 m=1
**.ends

* expanding   symbol:  /home/madvlsi/Documents/current-output-dac-vlsi/schematics/mux.sym # of
*+ pins=4
** sym_path: dac/schematics/mux.sym
** sch_path: dac/schematics/mux.sch
.subckt mux A B Y S
*.ipin A
*.ipin B
*.ipin S
*.opin Y
XM1 A S Y VDD sky130_fd_pr__pfet_01v8 L=0.15 W=1 nf=1 ad='int((nf+1)/2) * W/nf * 0.29' as='int((nf+2)/2) * W/nf * 0.29'
+ pd='2*int((nf+1)/2) * (W/nf + 0.29)' ps='2*int((nf+2)/2) * (W/nf + 0.29)' nrd='0.29 / W' nrs='0.29 / W'
+ sa=0 sb=0 sd=0 mult=1 m=1
XM3 net1 S VDD VDD sky130_fd_pr__pfet_01v8 L=0.15 W=1 nf=1 ad='int((nf+1)/2) * W/nf * 0.29' as='int((nf+2)/2) * W/nf * 0.29'
+ pd='2*int((nf+1)/2) * (W/nf + 0.29)' ps='2*int((nf+2)/2) * (W/nf + 0.29)' nrd='0.29 / W' nrs='0.29 / W'
+ sa=0 sb=0 sd=0 mult=1 m=1
XM4 net1 S GND GND sky130_fd_pr__nfet_01v8 L=0.15 W=1 nf=1 ad='int((nf+1)/2) * W/nf * 0.29' as='int((nf+2)/2) * W/nf * 0.29'
+ pd='2*int((nf+1)/2) * (W/nf + 0.29)' ps='2*int((nf+2)/2) * (W/nf + 0.29)' nrd='0.29 / W' nrs='0.29 / W'
+ sa=0 sb=0 sd=0 mult=1 m=1
XM5 A net1 Y GND sky130_fd_pr__nfet_01v8 L=0.15 W=1 nf=1 ad='int((nf+1)/2) * W/nf * 0.29' as='int((nf+2)/2) * W/nf * 0.29'
+ pd='2*int((nf+1)/2) * (W/nf + 0.29)' ps='2*int((nf+2)/2) * (W/nf + 0.29)' nrd='0.29 / W' nrs='0.29 / W'
+ sa=0 sb=0 sd=0 mult=1 m=1
XM2 B net1 Y VDD sky130_fd_pr__pfet_01v8 L=0.15 W=1 nf=1 ad='int((nf+1)/2) * W/nf * 0.29' as='int((nf+2)/2) * W/nf * 0.29'
+ pd='2*int((nf+1)/2) * (W/nf + 0.29)' ps='2*int((nf+2)/2) * (W/nf + 0.29)' nrd='0.29 / W' nrs='0.29 / W'
+ sa=0 sb=0 sd=0 mult=1 m=1
XM6 B S Y GND sky130_fd_pr__nfet_01v8 L=0.15 W=1 nf=1 ad='int((nf+1)/2) * W/nf * 0.29' as='int((nf+2)/2) * W/nf * 0.29'
+ pd='2*int((nf+1)/2) * (W/nf + 0.29)' ps='2*int((nf+2)/2) * (W/nf + 0.29)' nrd='0.29 / W' nrs='0.29 / W'
+ sa=0 sb=0 sd=0 mult=1 m=1
.ends

.GLOBAL VDD
.GLOBAL GND
.end
